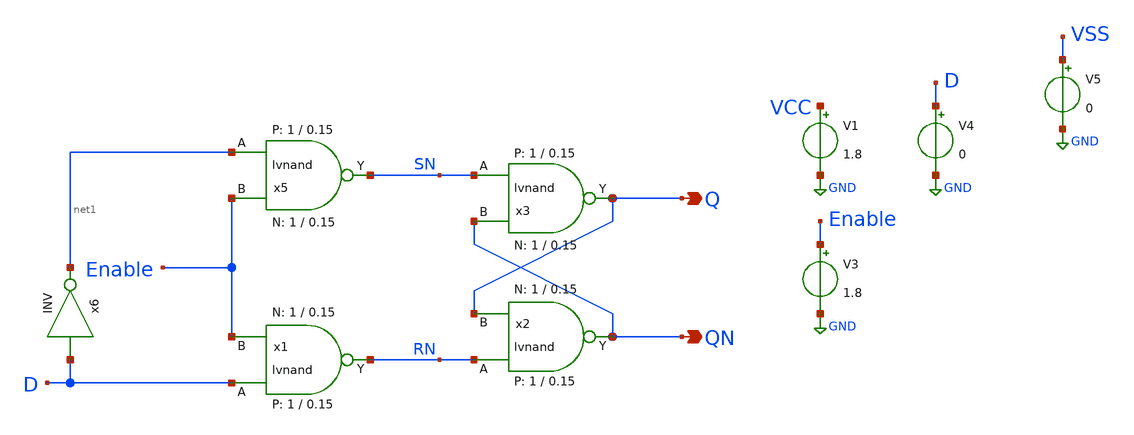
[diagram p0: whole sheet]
** sch_path: xschem/digital_prims/mem_test.sch
* Copyright 2021 Stefan Frederik Schippers
* Licensed under the Apache License, Version 2.0 (the "License");
* you may not use this file except in compliance with the License.
* You may obtain a copy of the License at
* https://www.apache.org/licenses/LICENSE-2.0
* Unless required by applicable law or agreed to in writing, software
* distributed under the License is distributed on an "AS IS" BASIS,
* WITHOUT WARRANTIES OR CONDITIONS OF ANY KIND, either express or implied.
* See the License for the specific language governing permissions and
* limitations under the License.
**.subckt mem_test Q QN
*.opin Q
*.opin QN
V1 VCC GND 1.8
V3 Enable GND 1.8
x5 net1 Enable SN VCC VSS lvnand WidthN=1 LenN=0.15 WidthP=1 LenP=0.15 m=1
x1 D Enable RN VCC VSS lvnand WidthN=1 LenN=0.15 WidthP=1 LenP=0.15 m=1
x2 RN Q QN VCC VSS lvnand WidthN=1 LenN=0.15 WidthP=1 LenP=0.15 m=1
x3 SN QN Q VCC VSS lvnand WidthN=1 LenN=0.15 WidthP=1 LenP=0.15 m=1
V4 D GND 0
V5 VSS GND 0
x6 net1 D VCC VSS VCC VSS INV
**** begin user architecture code

** opencircuitdesign pdks install
.lib $::SKYWATER_MODELS/sky130.lib.spice tt_mm


**** end user architecture code
**.ends

* expanding   symbol:  sky130_tests/lvnand.sym # of pins=3
** sym_path: sky130_tests/lvnand.sym
** sch_path: sky130_tests/lvnand.sch
.subckt lvnand A B Y VCCPIN VSSPIN  WidthN=1 LenN=0.15 WidthP=1 LenP=0.15
*.ipin A
*.ipin B
*.opin Y
XM1 Y B S VSSPIN sky130_fd_pr__nfet_01v8 L=LenN W=WidthN nf=1 ad='int((nf+1)/2) * W/nf * 0.29' as='int((nf+2)/2) * W/nf * 0.29'
+ pd='2*int((nf+1)/2) * (W/nf + 0.29)' ps='2*int((nf+2)/2) * (W/nf + 0.29)' nrd='0.29 / W' nrs='0.29 / W'
+ sa=0 sb=0 sd=0 mult=1 m=1
XM2 Y A VCCPIN VCCPIN sky130_fd_pr__pfet_01v8 L=LenP W=WidthP nf=1 ad='int((nf+1)/2) * W/nf * 0.29' as='int((nf+2)/2) * W/nf * 0.29'
+ pd='2*int((nf+1)/2) * (W/nf + 0.29)' ps='2*int((nf+2)/2) * (W/nf + 0.29)' nrd='0.29 / W' nrs='0.29 / W'
+ sa=0 sb=0 sd=0 mult=1 m=1
XM3 Y B VCCPIN VCCPIN sky130_fd_pr__pfet_01v8 L=LenP W=WidthP nf=1 ad='int((nf+1)/2) * W/nf * 0.29' as='int((nf+2)/2) * W/nf * 0.29'
+ pd='2*int((nf+1)/2) * (W/nf + 0.29)' ps='2*int((nf+2)/2) * (W/nf + 0.29)' nrd='0.29 / W' nrs='0.29 / W'
+ sa=0 sb=0 sd=0 mult=1 m=1
XM4 S A VSSPIN VSSPIN sky130_fd_pr__nfet_01v8 L=LenN W=WidthN nf=1 ad='int((nf+1)/2) * W/nf * 0.29' as='int((nf+2)/2) * W/nf * 0.29'
+ pd='2*int((nf+1)/2) * (W/nf + 0.29)' ps='2*int((nf+2)/2) * (W/nf + 0.29)' nrd='0.29 / W' nrs='0.29 / W'
+ sa=0 sb=0 sd=0 mult=1 m=1
.ends

.GLOBAL GND
**** begin user architecture code

* .option SCALE=1e-6
.option method=gear seed=12
.param L=0.15
.param W=0.5

vd d 0 0
vg g 0 0
.control
tran 1ms 50ms
plot v(Q)
.endc





**** end user architecture code
.end
